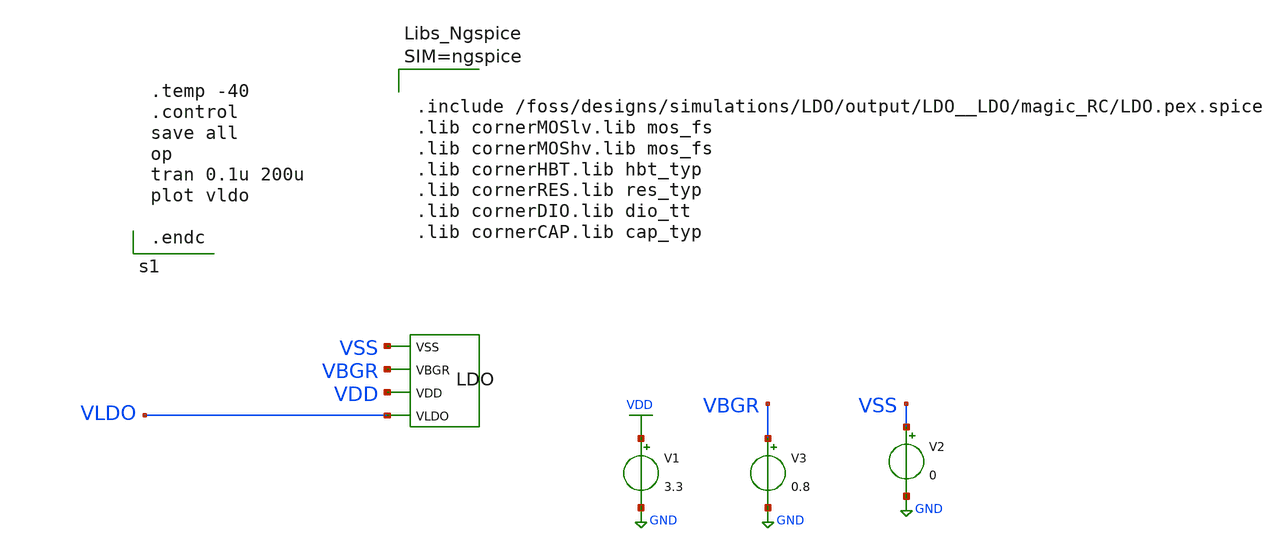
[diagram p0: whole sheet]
** sch_path: dependencies/LDO/LDO-main/testbenches/corners/xschem/ldo_post_layout_sim_fs_m40C.sch
**.subckt ldo_post_layout_sim_fs_m40C
V1 VDD GND 3.3
V3 VBGR GND 0.8
V2 VSS GND 0
X1 VSS VBGR VDD VLDO LDO
**** begin user architecture code



.include /foss/designs/simulations/LDO/output/LDO__LDO/magic_RC/LDO.pex.spice
.lib cornerMOSlv.lib mos_fs
.lib cornerMOShv.lib mos_fs
.lib cornerHBT.lib hbt_typ
.lib cornerRES.lib res_typ
.lib cornerDIO.lib dio_tt
.lib cornerCAP.lib cap_typ





.temp -40
.control
save all
op
tran 0.1u 200u
plot vldo

.endc

**** end user architecture code
**.ends
.GLOBAL GND
.GLOBAL VDD
.end
